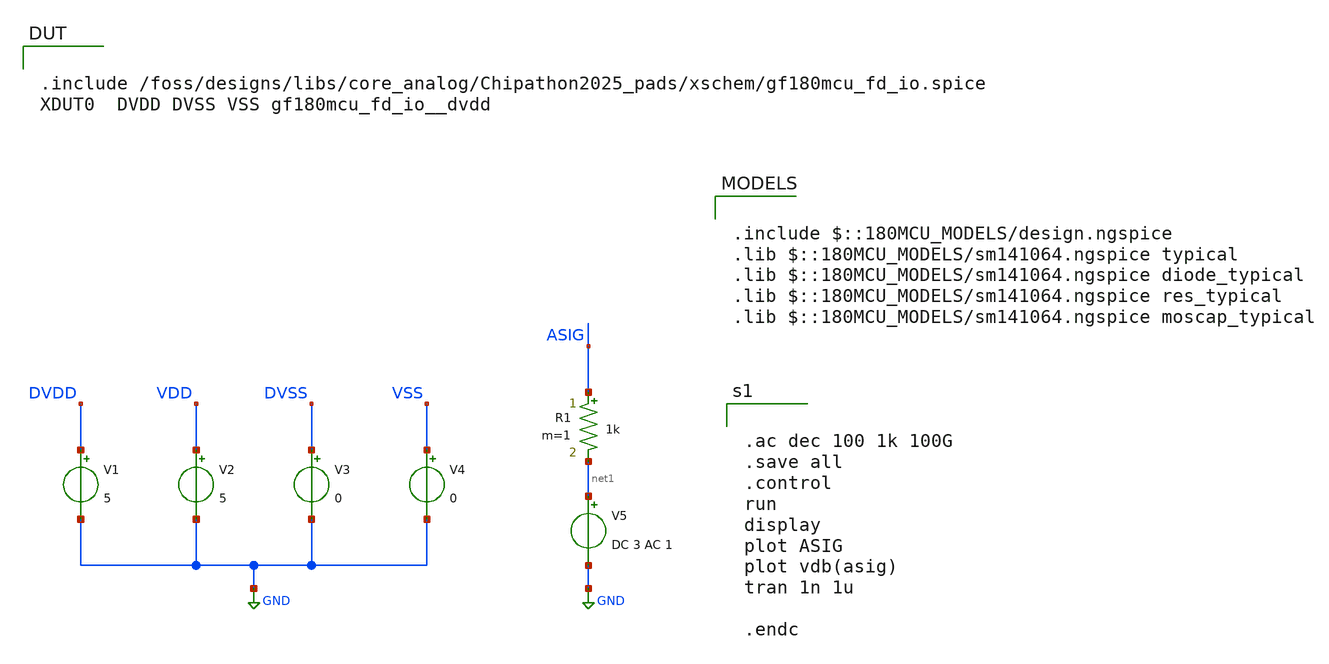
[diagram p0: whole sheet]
** sch_path: designs/libs/core_analog/Chipathon2025_pads/xschem/dvdd_AC_tb.sch
**.subckt dvdd_AC_tb
V1 DVDD GND 5
V2 VDD GND 5
V3 DVSS GND 0
V4 VSS GND 0
V5 net1 GND DC 3 AC 1
R1 ASIG net1 1k m=1
**** begin user architecture code

.include /foss/designs/libs/core_analog/Chipathon2025_pads/xschem/gf180mcu_fd_io.spice
XDUT0  DVDD DVSS VSS gf180mcu_fd_io__dvdd


.include $::180MCU_MODELS/design.ngspice
.lib $::180MCU_MODELS/sm141064.ngspice typical
.lib $::180MCU_MODELS/sm141064.ngspice diode_typical
.lib $::180MCU_MODELS/sm141064.ngspice res_typical
.lib $::180MCU_MODELS/sm141064.ngspice moscap_typical



.ac dec 100 1k 100G
.save all
.control
run
display
plot ASIG
plot vdb(asig)
tran 1n 1u

.endc


**** end user architecture code
**.ends
.GLOBAL GND
.end
